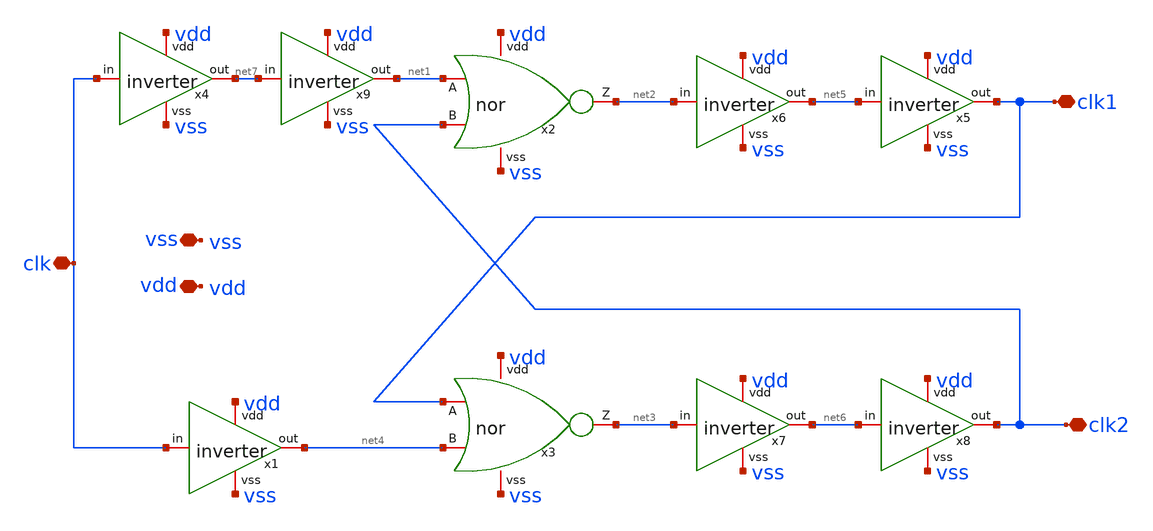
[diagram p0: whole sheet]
** sch_path: designs/sch/clockgen.sch
**.subckt clockgen vss vdd clk1 clk2 clk
*.iopin vss
*.iopin vdd
*.iopin clk1
*.iopin clk2
*.iopin clk
x1 vdd net4 clk vss inverter
x2 vdd net2 net1 clk2 vss nor
x3 vdd net3 clk1 net4 vss nor
x4 vdd net7 clk vss inverter
x6 vdd net5 net2 vss inverter
x7 vdd net6 net3 vss inverter
x5 vdd clk1 net5 vss inverter
x8 vdd clk2 net6 vss inverter
x9 vdd net1 net7 vss inverter
**.ends

* expanding   symbol:  /foss/designs/sch/inverter.sym # of pins=4
** sym_path: designs/inverter.sym
** sch_path: designs/inverter.sch
.subckt inverter vdd out in vss
*.iopin out
*.iopin vss
*.iopin vdd
*.iopin in
XM2 out in vss vss sky130_fd_pr__nfet_01v8 L=0.15 W=0.75 nf=1 ad='int((nf+1)/2) * W/nf * 0.29' as='int((nf+2)/2) * W/nf * 0.29'
+ pd='2*int((nf+1)/2) * (W/nf + 0.29)' ps='2*int((nf+2)/2) * (W/nf + 0.29)' nrd='0.29 / W' nrs='0.29 / W'
+ sa=0 sb=0 sd=0 mult=1 m=1
XM1 out in vdd vdd sky130_fd_pr__pfet_01v8 L=0.15 W=1.5 nf=1 ad='int((nf+1)/2) * W/nf * 0.29' as='int((nf+2)/2) * W/nf * 0.29'
+ pd='2*int((nf+1)/2) * (W/nf + 0.29)' ps='2*int((nf+2)/2) * (W/nf + 0.29)' nrd='0.29 / W' nrs='0.29 / W'
+ sa=0 sb=0 sd=0 mult=1 m=1
.ends


* expanding   symbol:  /foss/designs/sch/nor.sym # of pins=5
** sym_path: designs/sch/nor.sym
** sch_path: designs/sch/nor.sch
.subckt nor vdd Z A B vss
*.iopin A
*.iopin B
*.iopin vdd
*.iopin Z
*.iopin vss
XM1 Z A vss vss sky130_fd_pr__nfet_01v8 L=0.15 W=0.75 nf=1 ad='int((nf+1)/2) * W/nf * 0.29' as='int((nf+2)/2) * W/nf * 0.29'
+ pd='2*int((nf+1)/2) * (W/nf + 0.29)' ps='2*int((nf+2)/2) * (W/nf + 0.29)' nrd='0.29 / W' nrs='0.29 / W'
+ sa=0 sb=0 sd=0 mult=1 m=1
XM4 net1 B vdd vdd sky130_fd_pr__pfet_01v8 L=0.15 W=3 nf=1 ad='int((nf+1)/2) * W/nf * 0.29' as='int((nf+2)/2) * W/nf * 0.29'
+ pd='2*int((nf+1)/2) * (W/nf + 0.29)' ps='2*int((nf+2)/2) * (W/nf + 0.29)' nrd='0.29 / W' nrs='0.29 / W'
+ sa=0 sb=0 sd=0 mult=1 m=1
XM2 Z B vss vss sky130_fd_pr__nfet_01v8 L=0.15 W=0.75 nf=1 ad='int((nf+1)/2) * W/nf * 0.29' as='int((nf+2)/2) * W/nf * 0.29'
+ pd='2*int((nf+1)/2) * (W/nf + 0.29)' ps='2*int((nf+2)/2) * (W/nf + 0.29)' nrd='0.29 / W' nrs='0.29 / W'
+ sa=0 sb=0 sd=0 mult=1 m=1
XM3 Z A net1 vdd sky130_fd_pr__pfet_01v8 L=0.15 W=3 nf=1 ad='int((nf+1)/2) * W/nf * 0.29' as='int((nf+2)/2) * W/nf * 0.29'
+ pd='2*int((nf+1)/2) * (W/nf + 0.29)' ps='2*int((nf+2)/2) * (W/nf + 0.29)' nrd='0.29 / W' nrs='0.29 / W'
+ sa=0 sb=0 sd=0 mult=1 m=1
.ends

.end
